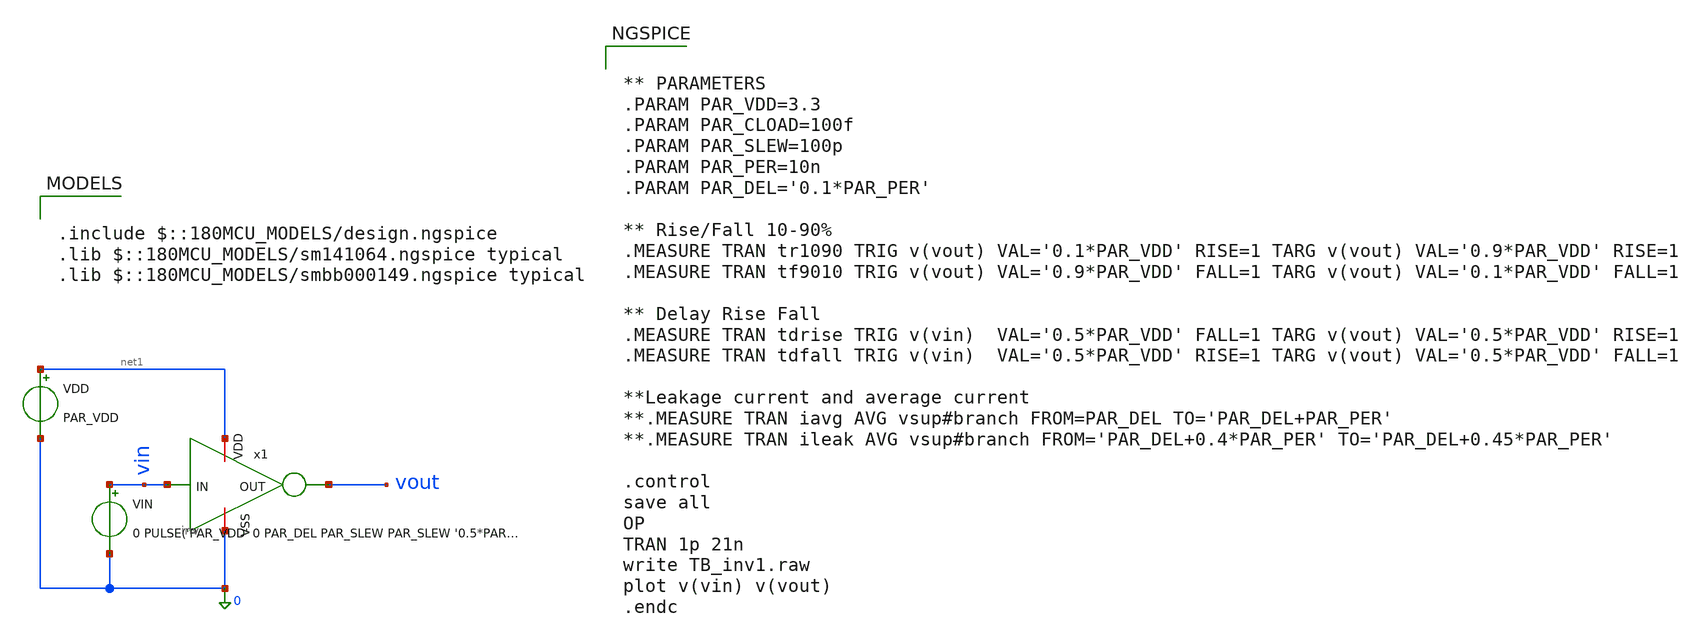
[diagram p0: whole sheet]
** sch_path: schematics/logic-gates/inv/inv_tb.sch
**.subckt inv_tb
VIN vin 0 0 PULSE('PAR_VDD' 0 PAR_DEL PAR_SLEW PAR_SLEW '0.5*PAR_PER' '1.0*PAR_PER')
VDD net1 0 PAR_VDD
x1 net1 vin vout 0 inv
**** begin user architecture code

.include $::180MCU_MODELS/design.ngspice
.lib $::180MCU_MODELS/sm141064.ngspice typical
.lib $::180MCU_MODELS/smbb000149.ngspice typical



** PARAMETERS
.PARAM PAR_VDD=3.3
.PARAM PAR_CLOAD=100f
.PARAM PAR_SLEW=100p
.PARAM PAR_PER=10n
.PARAM PAR_DEL='0.1*PAR_PER'

** Rise/Fall 10-90%
.MEASURE TRAN tr1090 TRIG v(vout) VAL='0.1*PAR_VDD' RISE=1 TARG v(vout) VAL='0.9*PAR_VDD' RISE=1
.MEASURE TRAN tf9010 TRIG v(vout) VAL='0.9*PAR_VDD' FALL=1 TARG v(vout) VAL='0.1*PAR_VDD' FALL=1

** Delay Rise Fall
.MEASURE TRAN tdrise TRIG v(vin)  VAL='0.5*PAR_VDD' FALL=1 TARG v(vout) VAL='0.5*PAR_VDD' RISE=1
.MEASURE TRAN tdfall TRIG v(vin)  VAL='0.5*PAR_VDD' RISE=1 TARG v(vout) VAL='0.5*PAR_VDD' FALL=1

**Leakage current and average current
**.MEASURE TRAN iavg AVG vsup#branch FROM=PAR_DEL TO='PAR_DEL+PAR_PER'
**.MEASURE TRAN ileak AVG vsup#branch FROM='PAR_DEL+0.4*PAR_PER' TO='PAR_DEL+0.45*PAR_PER'

.control
save all
OP
TRAN 1p 21n
write TB_inv1.raw
plot v(vin) v(vout)
.endc



**** end user architecture code
**.ends

* expanding   symbol:  schematics/logic-gates/inv/inv.sym # of pins=4
** sym_path: schematics/logic-gates/inv/inv.sym
** sch_path: schematics/logic-gates/inv/inv.sch
.subckt inv VDD IN OUT VSS
*.ipin IN
*.opin OUT
*.iopin VDD
*.iopin VSS
XM1 OUT IN VSS VSS nfet_03v3 L=0.28u W=0.22u nf=1 ad='int((nf+1)/2) * W/nf * 0.18u' as='int((nf+2)/2) * W/nf * 0.18u'
+ pd='2*int((nf+1)/2) * (W/nf + 0.18u)' ps='2*int((nf+2)/2) * (W/nf + 0.18u)' nrd='0.18u / W' nrs='0.18u / W'
+ sa=0 sb=0 sd=0 m=1
XM2 OUT IN VDD VDD pfet_03v3 L=0.28u W=0.22u nf=1 ad='int((nf+1)/2) * W/nf * 0.18u' as='int((nf+2)/2) * W/nf * 0.18u'
+ pd='2*int((nf+1)/2) * (W/nf + 0.18u)' ps='2*int((nf+2)/2) * (W/nf + 0.18u)' nrd='0.18u / W' nrs='0.18u / W'
+ sa=0 sb=0 sd=0 m=1
.ends

.end
